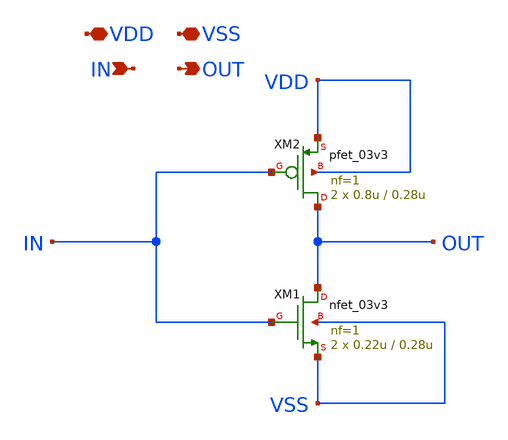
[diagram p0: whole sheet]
** sch_path: Clock_Generator_PAKISTAN_02/Schematics/Delayed_INV.sch
**.subckt Delayed_INV VDD VSS IN OUT
*.iopin VDD
*.iopin VSS
*.ipin IN
*.opin OUT
XM1 OUT IN VSS VSS nfet_03v3 L=0.28u W=0.22u nf=1 ad='int((nf+1)/2) * W/nf * 0.18u' as='int((nf+2)/2) * W/nf * 0.18u'
+ pd='2*int((nf+1)/2) * (W/nf + 0.18u)' ps='2*int((nf+2)/2) * (W/nf + 0.18u)' nrd='0.18u / W' nrs='0.18u / W'
+ sa=0 sb=0 sd=0 m=2
XM2 OUT IN VDD VDD pfet_03v3 L=0.28u W=0.8u nf=1 ad='int((nf+1)/2) * W/nf * 0.18u' as='int((nf+2)/2) * W/nf * 0.18u'
+ pd='2*int((nf+1)/2) * (W/nf + 0.18u)' ps='2*int((nf+2)/2) * (W/nf + 0.18u)' nrd='0.18u / W' nrs='0.18u / W'
+ sa=0 sb=0 sd=0 m=2
**.ends
.end
